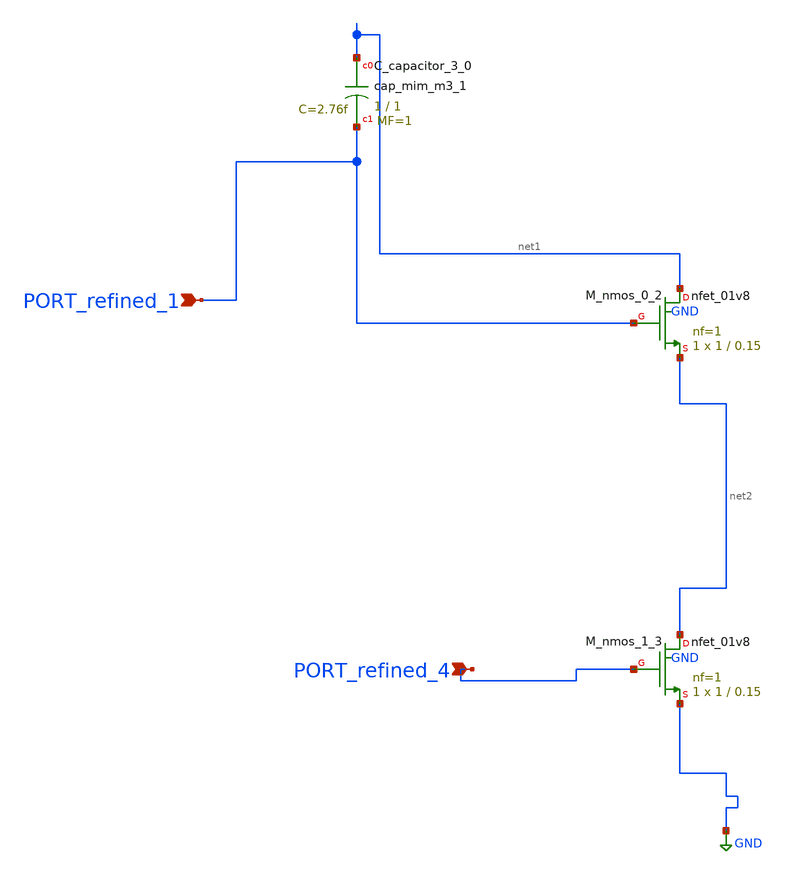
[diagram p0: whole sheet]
** sch_path: schematics/AMSNet/183.sch
**.subckt 183 PORT_refined_4 PORT_refined_1
*.ipin PORT_refined_4
*.ipin PORT_refined_1
XC_capacitor_3_0 net1 PORT_refined_1 sky130_fd_pr__cap_mim_m3_1 W=1 L=1 MF=1 m=1
XM_nmos_0_2 net1 PORT_refined_1 net2 GND sky130_fd_pr__nfet_01v8 L=0.15 W=1 nf=1 ad='int((1 + 1)/2) * 1 / 1 * 0.29'
+ as='int((1 + 2)/2) * 1 / 1 * 0.29' pd='2*int((1 + 1)/2) * (1 / 1 + 0.29)' ps='2*int((1 + 2)/2) * (1 / 1 + 0.29)'
+ nrd='0.29 / 1 ' nrs='0.29 / 1 ' sa=0 sb=0 sd=0 mult=1 m=1
XM_nmos_1_3 net2 PORT_refined_4 GND GND sky130_fd_pr__nfet_01v8 L=0.15 W=1 nf=1 ad='int((1 + 1)/2) * 1 / 1 * 0.29'
+ as='int((1 + 2)/2) * 1 / 1 * 0.29' pd='2*int((1 + 1)/2) * (1 / 1 + 0.29)' ps='2*int((1 + 2)/2) * (1 / 1 + 0.29)'
+ nrd='0.29 / 1 ' nrs='0.29 / 1 ' sa=0 sb=0 sd=0 mult=1 m=1
**.ends
.GLOBAL GND
.end
